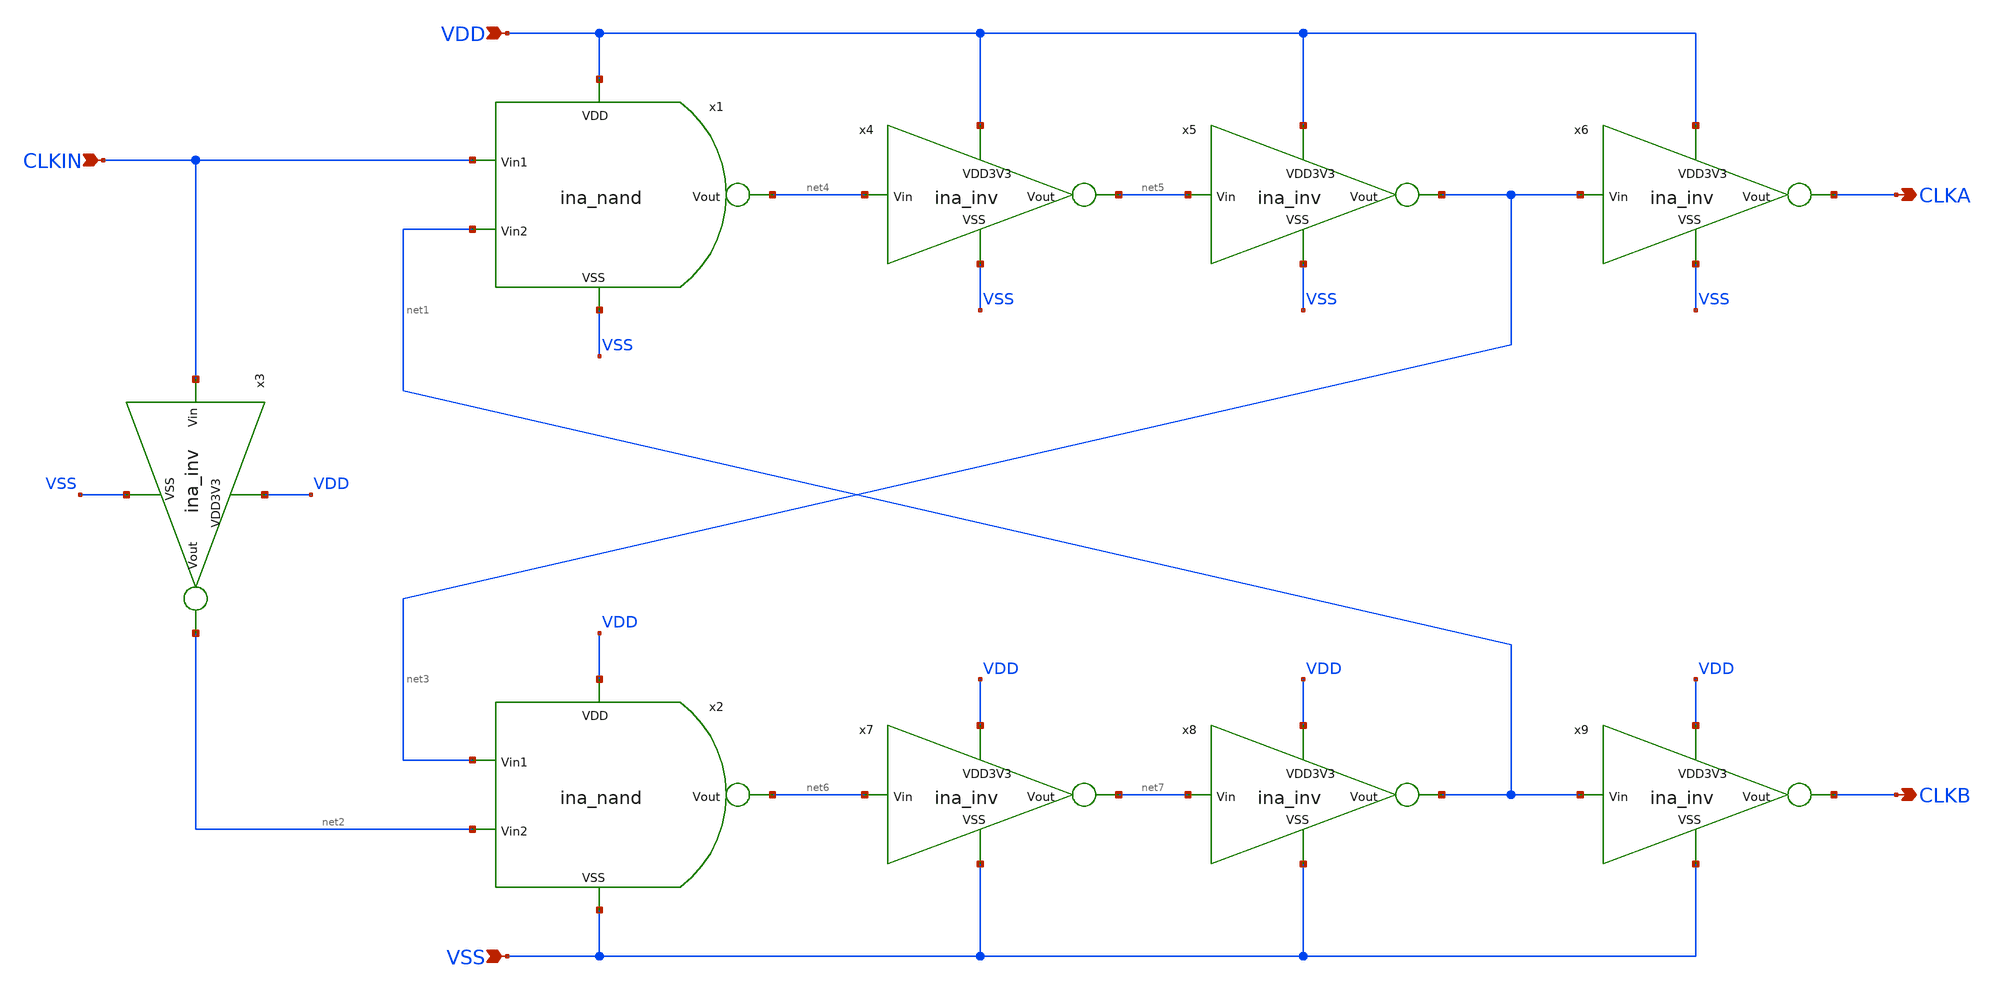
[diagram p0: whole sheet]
** sch_path: designs/libs/core_ina/ina_clockgen/ina_clockgen.sch
**.subckt ina_clockgen CLKIN VDD VSS CLKA CLKB
*.ipin CLKIN
*.ipin VDD
*.ipin VSS
*.opin CLKA
*.opin CLKB
x1 VDD net4 CLKIN net1 VSS ina_nand
x2 VDD net6 net3 net2 VSS ina_nand
x3 VDD CLKIN net2 VSS ina_inv
x4 VDD net4 net5 VSS ina_inv
x5 VDD net5 net3 VSS ina_inv
x6 VDD net3 CLKA VSS ina_inv
x7 VDD net6 net7 VSS ina_inv
x8 VDD net7 net1 VSS ina_inv
x9 VDD net1 CLKB VSS ina_inv
**.ends

* expanding   symbol:  libs/core_ina/ina_nand/ina_nand.sym # of pins=5
** sym_path: designs/libs/core_ina/ina_nand/ina_nand.sym
** sch_path: designs/libs/core_ina/ina_nand/ina_nand.sch
.subckt ina_nand VDD Vout Vin1 Vin2 VSS
*.ipin VDD
*.ipin Vin1
*.ipin Vin2
*.ipin VSS
*.opin Vout
XMN1 Vout Vin1 VDD VDD pfet_03v3 L=0.28u W=2u nf=1 ad='int((nf+1)/2) * W/nf * 0.18u' as='int((nf+2)/2) * W/nf * 0.18u'
+ pd='2*int((nf+1)/2) * (W/nf + 0.18u)' ps='2*int((nf+2)/2) * (W/nf + 0.18u)' nrd='0.18u / W' nrs='0.18u / W'
+ sa=0 sb=0 sd=0 m=1
XMN2 Vout Vin2 VDD VDD pfet_03v3 L=0.28u W=2u nf=1 ad='int((nf+1)/2) * W/nf * 0.18u' as='int((nf+2)/2) * W/nf * 0.18u'
+ pd='2*int((nf+1)/2) * (W/nf + 0.18u)' ps='2*int((nf+2)/2) * (W/nf + 0.18u)' nrd='0.18u / W' nrs='0.18u / W'
+ sa=0 sb=0 sd=0 m=1
XMN3 Vout Vin1 net1 VSS nfet_03v3 L=0.28u W=2u nf=1 ad='int((nf+1)/2) * W/nf * 0.18u' as='int((nf+2)/2) * W/nf * 0.18u'
+ pd='2*int((nf+1)/2) * (W/nf + 0.18u)' ps='2*int((nf+2)/2) * (W/nf + 0.18u)' nrd='0.18u / W' nrs='0.18u / W'
+ sa=0 sb=0 sd=0 m=1
XMN4 net1 Vin2 VSS VSS nfet_03v3 L=0.28u W=2u nf=1 ad='int((nf+1)/2) * W/nf * 0.18u' as='int((nf+2)/2) * W/nf * 0.18u'
+ pd='2*int((nf+1)/2) * (W/nf + 0.18u)' ps='2*int((nf+2)/2) * (W/nf + 0.18u)' nrd='0.18u / W' nrs='0.18u / W'
+ sa=0 sb=0 sd=0 m=1
.ends


* expanding   symbol:  libs/core_ina/ina_inv/ina_inv.sym # of pins=4
** sym_path: designs/libs/core_ina/ina_inv/ina_inv.sym
** sch_path: designs/libs/core_ina/ina_inv/ina_inv.sch
.subckt ina_inv VDD3V3 Vin Vout VSS
*.ipin VDD3V3
*.ipin VSS
*.ipin Vin
*.opin Vout
XMI1 Vout Vin VDD3V3 VDD3V3 pfet_03v3 L=0.28u W=2u nf=1 ad='int((nf+1)/2) * W/nf * 0.18u' as='int((nf+2)/2) * W/nf * 0.18u'
+ pd='2*int((nf+1)/2) * (W/nf + 0.18u)' ps='2*int((nf+2)/2) * (W/nf + 0.18u)' nrd='0.18u / W' nrs='0.18u / W'
+ sa=0 sb=0 sd=0 m=1
XMI2 Vout Vin VSS VSS nfet_03v3 L=0.28u W=1u nf=1 ad='int((nf+1)/2) * W/nf * 0.18u' as='int((nf+2)/2) * W/nf * 0.18u'
+ pd='2*int((nf+1)/2) * (W/nf + 0.18u)' ps='2*int((nf+2)/2) * (W/nf + 0.18u)' nrd='0.18u / W' nrs='0.18u / W'
+ sa=0 sb=0 sd=0 m=1
.ends

.end
